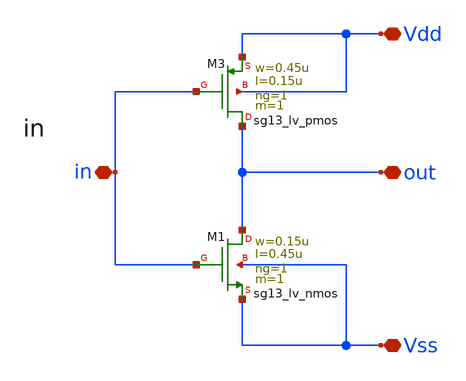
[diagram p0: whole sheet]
** sch_path: design/blocks/inversor/schematic/inversor.sch
**.subckt inversor out Vdd Vss in
*.iopin out
*.iopin Vdd
*.iopin Vss
*.iopin in
XM3 out in Vdd Vdd sg13_lv_pmos w=0.45u l=0.15u ng=1 m=1 mm_ok=1
XM1 out in Vss Vss sg13_lv_nmos w=0.15u l=0.45u ng=1 m=1 mm_ok=1
**.ends
.end
